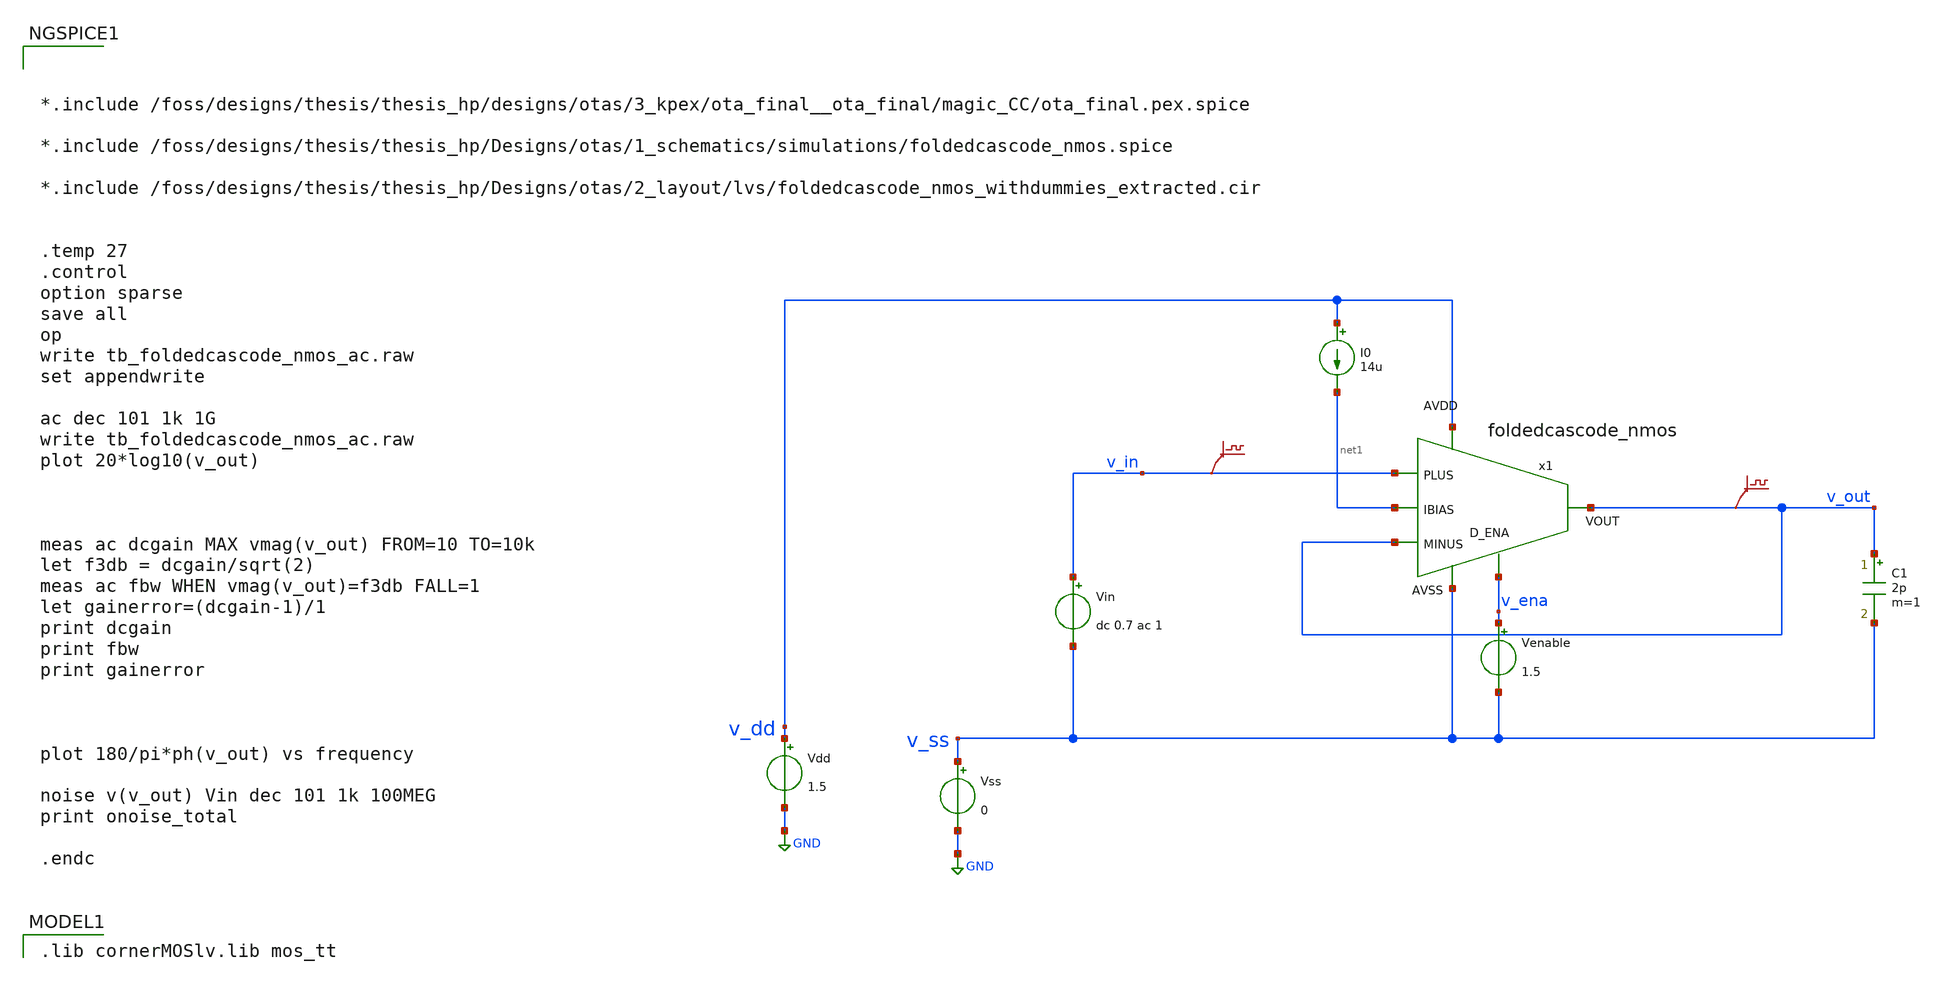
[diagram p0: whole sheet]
** sch_path: Designs/otas/1_schematics/tb_foldedcascode_nmos_ac.sch
* (c) 2025 Thesis_HP, Apache-2.0 license
**.subckt tb_foldedcascode_nmos_ac
Vss v_ss GND 0
Vdd v_dd GND 1.5
Vin v_in v_ss dc 0.7 ac 1
.save v(v_in)
I0 v_dd net1 14u
C1 v_out v_ss 2p m=1
.save v(v_out)
Venable v_ena v_ss 1.5
x1 v_dd net1 v_out v_out v_in v_ena v_ss foldedcascode_nmos
**** begin user architecture code
 .lib cornerMOSlv.lib mos_tt




*.include /foss/designs/thesis/thesis_hp/designs/otas/3_kpex/ota_final__ota_final/magic_CC/ota_final.pex.spice

*.include /foss/designs/thesis/thesis_hp/Designs/otas/1_schematics/simulations/foldedcascode_nmos.spice

*.include /foss/designs/thesis/thesis_hp/Designs/otas/2_layout/lvs/foldedcascode_nmos_withdummies_extracted.cir


.temp 27
.control
option sparse
save all
op
write tb_foldedcascode_nmos_ac.raw
set appendwrite

ac dec 101 1k 1G
write tb_foldedcascode_nmos_ac.raw
plot 20*log10(v_out)



meas ac dcgain MAX vmag(v_out) FROM=10 TO=10k
let f3db = dcgain/sqrt(2)
meas ac fbw WHEN vmag(v_out)=f3db FALL=1
let gainerror=(dcgain-1)/1
print dcgain
print fbw
print gainerror



plot 180/pi*ph(v_out) vs frequency

noise v(v_out) Vin dec 101 1k 100MEG
print onoise_total

.endc


**** end user architecture code
**.ends
.GLOBAL GND
.end
